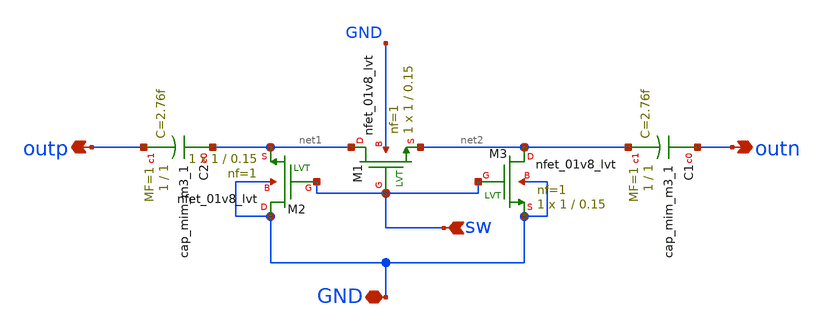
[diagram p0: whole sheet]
** sch_path: openfasoc/generators/lc-dco/xschem_rundir/swcap_verilog_ver.sch
**.subckt swcap_verilog_ver outn outp sw GND
*.opin outn
*.opin outp
*.ipin sw
*.iopin GND
XM1 net1 sw net2 GND sky130_fd_pr__nfet_01v8_lvt L=0.15 W=1 nf=1 ad='int((1 + 1)/2) * 1 / 1 * 0.29' as='int((1 + 2)/2) * 1 / 1 * 0.29'
+ pd='2*int((1 + 1)/2) * (1 / 1 + 0.29)' ps='2*int((1 + 2)/2) * (1 / 1 + 0.29)' nrd='0.29 / 1 ' nrs='0.29 / 1 '
+ sa=0 sb=0 sd=0 mult=1 m=1
XM2 GND sw net1 GND sky130_fd_pr__nfet_01v8_lvt L=0.15 W=1 nf=1 ad='int((1 + 1)/2) * 1 / 1 * 0.29' as='int((1 + 2)/2) * 1 / 1 * 0.29'
+ pd='2*int((1 + 1)/2) * (1 / 1 + 0.29)' ps='2*int((1 + 2)/2) * (1 / 1 + 0.29)' nrd='0.29 / 1 ' nrs='0.29 / 1 '
+ sa=0 sb=0 sd=0 mult=1 m=1
XM3 net2 sw GND GND sky130_fd_pr__nfet_01v8_lvt L=0.15 W=1 nf=1 ad='int((1 + 1)/2) * 1 / 1 * 0.29' as='int((1 + 2)/2) * 1 / 1 * 0.29'
+ pd='2*int((1 + 1)/2) * (1 / 1 + 0.29)' ps='2*int((1 + 2)/2) * (1 / 1 + 0.29)' nrd='0.29 / 1 ' nrs='0.29 / 1 '
+ sa=0 sb=0 sd=0 mult=1 m=1
XC1 outn net2 sky130_fd_pr__cap_mim_m3_1 W=1 L=1 MF=1 m=1
XC2 net1 outp sky130_fd_pr__cap_mim_m3_1 W=1 L=1 MF=1 m=1
**.ends
.end
